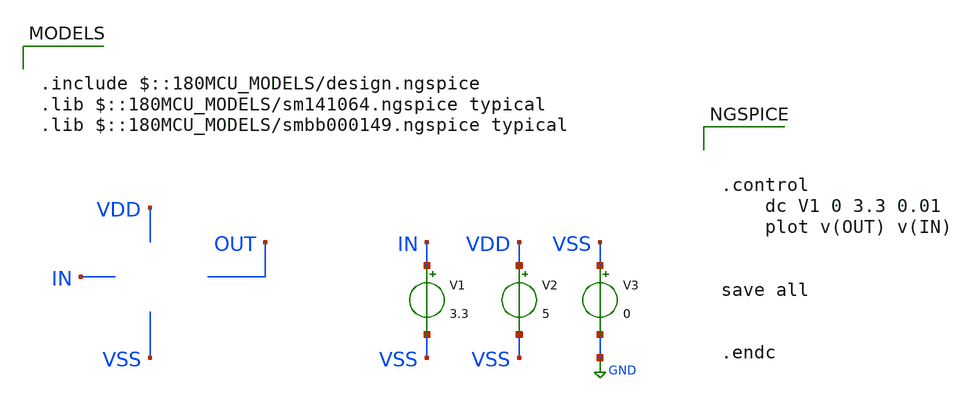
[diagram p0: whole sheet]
** sch_path: week01_mosfet_cmos/tugas2_cmos_inverter/cmos-inverter-tb.sch
**.subckt cmos-inverter-tb
V1 IN VSS 3.3
V2 VDD VSS 5
V3 VSS GND 0
**** begin user architecture code

.include $::180MCU_MODELS/design.ngspice
.lib $::180MCU_MODELS/sm141064.ngspice typical
.lib $::180MCU_MODELS/smbb000149.ngspice typical




.control
	dc V1 0 3.3 0.01
	plot v(OUT) v(IN)


save all


.endc


**** end user architecture code
**.ends
.GLOBAL GND
.end
